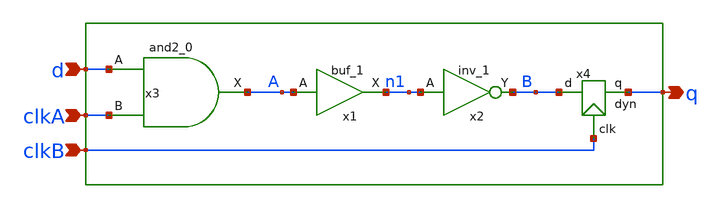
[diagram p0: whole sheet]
** sch_path: src/xe/test_cases/and_dyn_odd.sch
**.subckt and_dyn_odd d clkA q clkB
*.ipin d
*.ipin clkA
*.opin q
*.ipin clkB
x4 clkB q B dyn vcc=vss vss=vss
x1 A vss vss vcc vcc n1 sky130_fd_sc_hd__buf_1
x3 d clkA VGND VNB VPB VPWR A sky130_fd_sc_hd__and2_0
x2 n1 VGND VNB VPB VPWR B sky130_fd_sc_hd__inv_1
**.ends

* expanding   symbol:  yxt/dyn.sym # of pins=3
** sym_path: src/xe/test_cases/dyn.sym
** sch_path: src/xe/test_cases/dyn.sch
.subckt dyn clk q d  vcc=vss vss=vss
*.ipin clk
*.opin q
*.ipin d
x1 net1 vcc vcc vss vss q sky130_fd_sc_hd__inv_1
XM1 net1 d net2 net3 sky130_fd_pr__nfet_01v8 L=0.15 W=1 nf=1 ad='int((nf+1)/2) * W/nf * 0.29' as='int((nf+2)/2) * W/nf * 0.29'
+ pd='2*int((nf+1)/2) * (W/nf + 0.29)' ps='2*int((nf+2)/2) * (W/nf + 0.29)' nrd='0.29 / W' nrs='0.29 / W'
+ sa=0 sb=0 sd=0 mult=1 m=1
XM2 net1 q vcc net4 sky130_fd_pr__pfet_01v8 L=0.15 W=1 nf=1 ad='int((nf+1)/2) * W/nf * 0.29' as='int((nf+2)/2) * W/nf * 0.29'
+ pd='2*int((nf+1)/2) * (W/nf + 0.29)' ps='2*int((nf+2)/2) * (W/nf + 0.29)' nrd='0.29 / W' nrs='0.29 / W'
+ sa=0 sb=0 sd=0 mult=1 m=1
XM3 net1 clk vcc net5 sky130_fd_pr__pfet_01v8 L=0.15 W=1 nf=1 ad='int((nf+1)/2) * W/nf * 0.29' as='int((nf+2)/2) * W/nf * 0.29'
+ pd='2*int((nf+1)/2) * (W/nf + 0.29)' ps='2*int((nf+2)/2) * (W/nf + 0.29)' nrd='0.29 / W' nrs='0.29 / W'
+ sa=0 sb=0 sd=0 mult=1 m=1
XM4 net2 clk vss net6 sky130_fd_pr__nfet_01v8 L=0.15 W=1 nf=1 ad='int((nf+1)/2) * W/nf * 0.29' as='int((nf+2)/2) * W/nf * 0.29'
+ pd='2*int((nf+1)/2) * (W/nf + 0.29)' ps='2*int((nf+2)/2) * (W/nf + 0.29)' nrd='0.29 / W' nrs='0.29 / W'
+ sa=0 sb=0 sd=0 mult=1 m=1
.ends

.end
